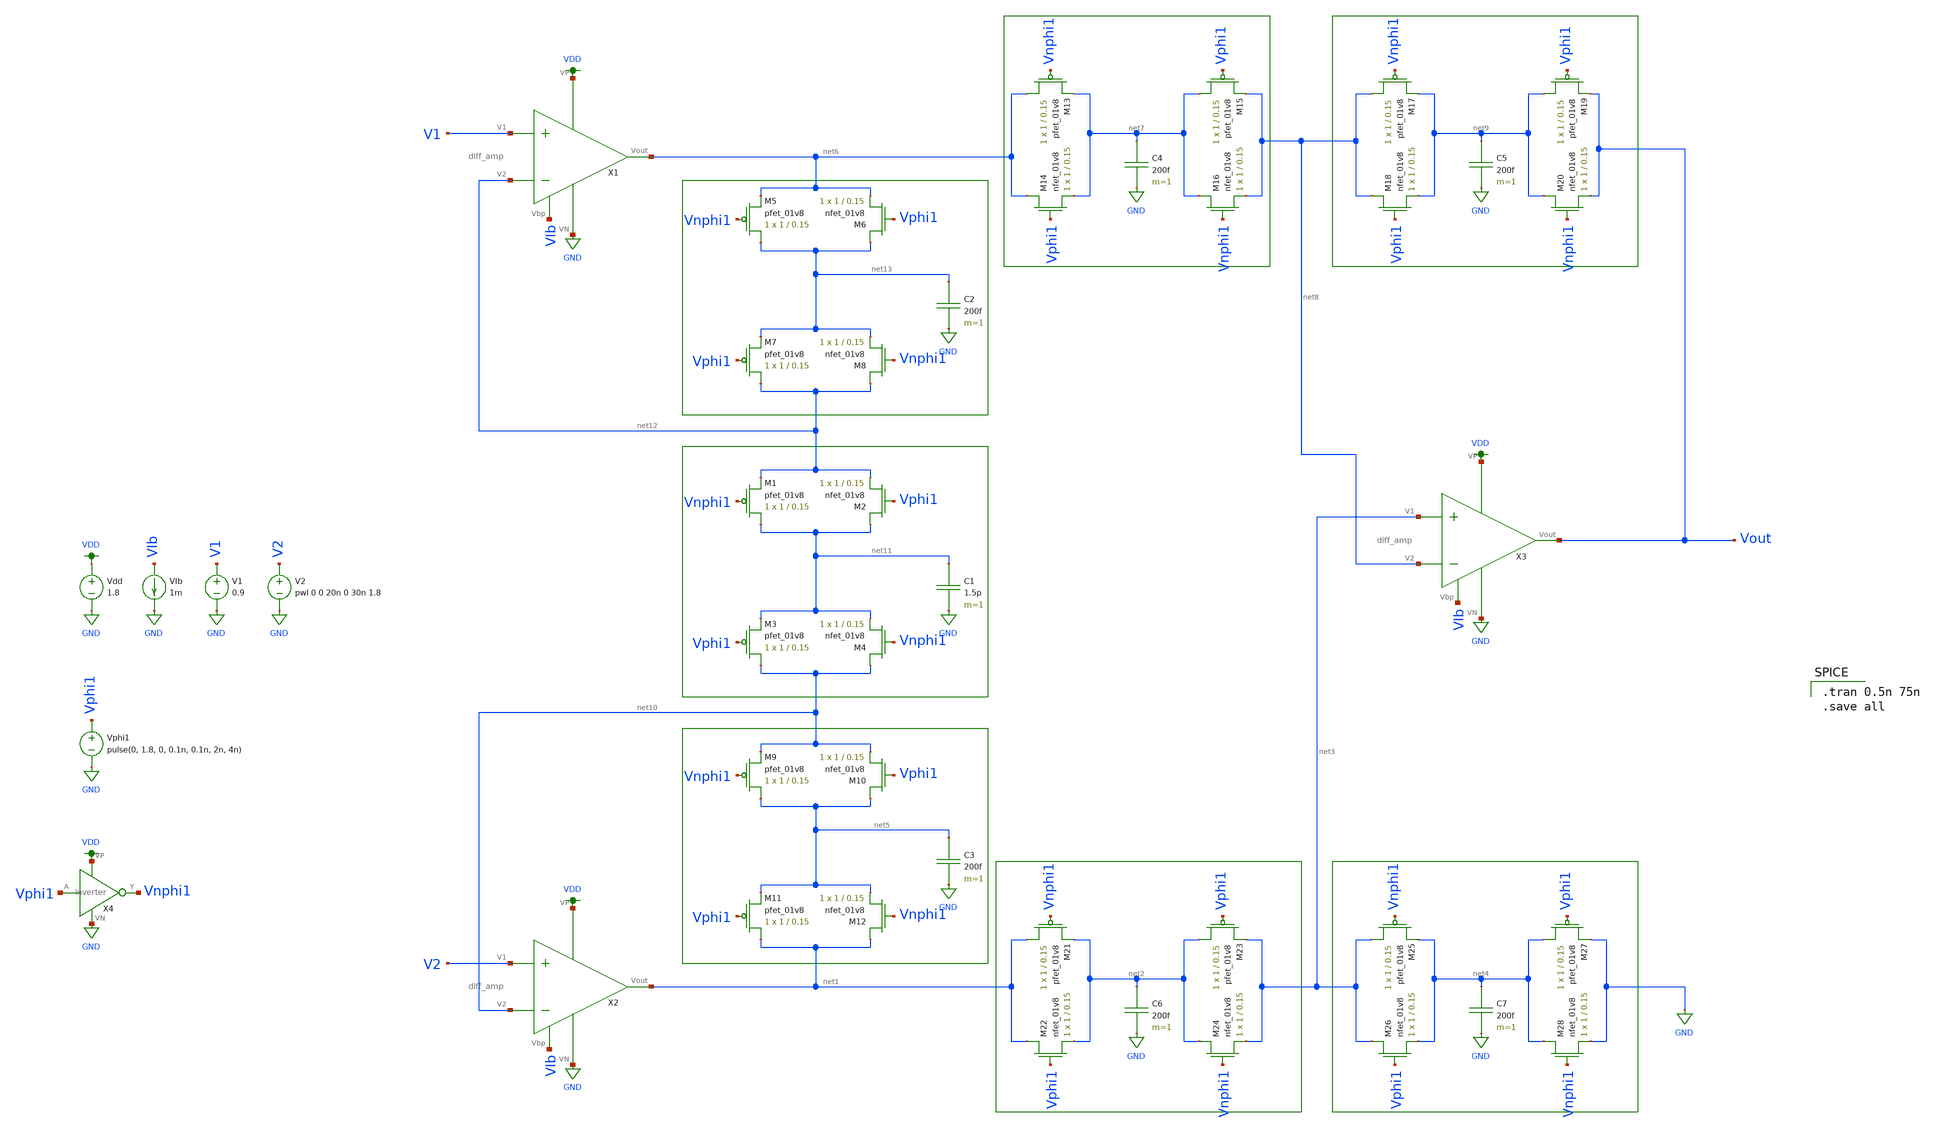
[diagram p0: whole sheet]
** sch_path: schematic/archive/alpha_amp.sch
**.subckt alpha_amp
X1 VDD VIb net6 V1 net12 GND diff_amp
X2 VDD VIb net1 V2 net10 GND diff_amp
X3 VDD VIb Vout net3 net8 GND diff_amp
XM1 net11 Vnphi1 net12 VDD sky130_fd_pr__pfet_01v8 L=0.15 W=1 nf=1 ad='int((nf+1)/2) * W/nf * 0.29' as='int((nf+2)/2) * W/nf * 0.29'
+ pd='2*int((nf+1)/2) * (W/nf + 0.29)' ps='2*int((nf+2)/2) * (W/nf + 0.29)' nrd='0.29 / W' nrs='0.29 / W'
+ sa=0 sb=0 sd=0 mult=1 m=1
XM2 net11 Vphi1 net12 GND sky130_fd_pr__nfet_01v8 L=0.15 W=1 nf=1 ad='int((nf+1)/2) * W/nf * 0.29' as='int((nf+2)/2) * W/nf * 0.29'
+ pd='2*int((nf+1)/2) * (W/nf + 0.29)' ps='2*int((nf+2)/2) * (W/nf + 0.29)' nrd='0.29 / W' nrs='0.29 / W'
+ sa=0 sb=0 sd=0 mult=1 m=1
C1 net11 GND 1.5p m=1
XM3 net10 Vphi1 net11 VDD sky130_fd_pr__pfet_01v8 L=0.15 W=1 nf=1 ad='int((nf+1)/2) * W/nf * 0.29' as='int((nf+2)/2) * W/nf * 0.29'
+ pd='2*int((nf+1)/2) * (W/nf + 0.29)' ps='2*int((nf+2)/2) * (W/nf + 0.29)' nrd='0.29 / W' nrs='0.29 / W'
+ sa=0 sb=0 sd=0 mult=1 m=1
XM4 net10 Vnphi1 net11 GND sky130_fd_pr__nfet_01v8 L=0.15 W=1 nf=1 ad='int((nf+1)/2) * W/nf * 0.29' as='int((nf+2)/2) * W/nf * 0.29'
+ pd='2*int((nf+1)/2) * (W/nf + 0.29)' ps='2*int((nf+2)/2) * (W/nf + 0.29)' nrd='0.29 / W' nrs='0.29 / W'
+ sa=0 sb=0 sd=0 mult=1 m=1
XM5 net13 Vnphi1 net6 VDD sky130_fd_pr__pfet_01v8 L=0.15 W=1 nf=1 ad='int((nf+1)/2) * W/nf * 0.29' as='int((nf+2)/2) * W/nf * 0.29'
+ pd='2*int((nf+1)/2) * (W/nf + 0.29)' ps='2*int((nf+2)/2) * (W/nf + 0.29)' nrd='0.29 / W' nrs='0.29 / W'
+ sa=0 sb=0 sd=0 mult=1 m=1
XM6 net13 Vphi1 net6 GND sky130_fd_pr__nfet_01v8 L=0.15 W=1 nf=1 ad='int((nf+1)/2) * W/nf * 0.29' as='int((nf+2)/2) * W/nf * 0.29'
+ pd='2*int((nf+1)/2) * (W/nf + 0.29)' ps='2*int((nf+2)/2) * (W/nf + 0.29)' nrd='0.29 / W' nrs='0.29 / W'
+ sa=0 sb=0 sd=0 mult=1 m=1
C2 net13 GND 200f m=1
XM7 net12 Vphi1 net13 VDD sky130_fd_pr__pfet_01v8 L=0.15 W=1 nf=1 ad='int((nf+1)/2) * W/nf * 0.29' as='int((nf+2)/2) * W/nf * 0.29'
+ pd='2*int((nf+1)/2) * (W/nf + 0.29)' ps='2*int((nf+2)/2) * (W/nf + 0.29)' nrd='0.29 / W' nrs='0.29 / W'
+ sa=0 sb=0 sd=0 mult=1 m=1
XM8 net12 Vnphi1 net13 GND sky130_fd_pr__nfet_01v8 L=0.15 W=1 nf=1 ad='int((nf+1)/2) * W/nf * 0.29' as='int((nf+2)/2) * W/nf * 0.29'
+ pd='2*int((nf+1)/2) * (W/nf + 0.29)' ps='2*int((nf+2)/2) * (W/nf + 0.29)' nrd='0.29 / W' nrs='0.29 / W'
+ sa=0 sb=0 sd=0 mult=1 m=1
XM9 net5 Vnphi1 net10 VDD sky130_fd_pr__pfet_01v8 L=0.15 W=1 nf=1 ad='int((nf+1)/2) * W/nf * 0.29' as='int((nf+2)/2) * W/nf * 0.29'
+ pd='2*int((nf+1)/2) * (W/nf + 0.29)' ps='2*int((nf+2)/2) * (W/nf + 0.29)' nrd='0.29 / W' nrs='0.29 / W'
+ sa=0 sb=0 sd=0 mult=1 m=1
XM10 net5 Vphi1 net10 GND sky130_fd_pr__nfet_01v8 L=0.15 W=1 nf=1 ad='int((nf+1)/2) * W/nf * 0.29' as='int((nf+2)/2) * W/nf * 0.29'
+ pd='2*int((nf+1)/2) * (W/nf + 0.29)' ps='2*int((nf+2)/2) * (W/nf + 0.29)' nrd='0.29 / W' nrs='0.29 / W'
+ sa=0 sb=0 sd=0 mult=1 m=1
C3 net5 GND 200f m=1
XM11 net1 Vphi1 net5 VDD sky130_fd_pr__pfet_01v8 L=0.15 W=1 nf=1 ad='int((nf+1)/2) * W/nf * 0.29' as='int((nf+2)/2) * W/nf * 0.29'
+ pd='2*int((nf+1)/2) * (W/nf + 0.29)' ps='2*int((nf+2)/2) * (W/nf + 0.29)' nrd='0.29 / W' nrs='0.29 / W'
+ sa=0 sb=0 sd=0 mult=1 m=1
XM12 net1 Vnphi1 net5 GND sky130_fd_pr__nfet_01v8 L=0.15 W=1 nf=1 ad='int((nf+1)/2) * W/nf * 0.29' as='int((nf+2)/2) * W/nf * 0.29'
+ pd='2*int((nf+1)/2) * (W/nf + 0.29)' ps='2*int((nf+2)/2) * (W/nf + 0.29)' nrd='0.29 / W' nrs='0.29 / W'
+ sa=0 sb=0 sd=0 mult=1 m=1
XM13 net6 Vnphi1 net7 VDD sky130_fd_pr__pfet_01v8 L=0.15 W=1 nf=1 ad='int((nf+1)/2) * W/nf * 0.29' as='int((nf+2)/2) * W/nf * 0.29'
+ pd='2*int((nf+1)/2) * (W/nf + 0.29)' ps='2*int((nf+2)/2) * (W/nf + 0.29)' nrd='0.29 / W' nrs='0.29 / W'
+ sa=0 sb=0 sd=0 mult=1 m=1
XM14 net6 Vphi1 net7 GND sky130_fd_pr__nfet_01v8 L=0.15 W=1 nf=1 ad='int((nf+1)/2) * W/nf * 0.29' as='int((nf+2)/2) * W/nf * 0.29'
+ pd='2*int((nf+1)/2) * (W/nf + 0.29)' ps='2*int((nf+2)/2) * (W/nf + 0.29)' nrd='0.29 / W' nrs='0.29 / W'
+ sa=0 sb=0 sd=0 mult=1 m=1
C4 net7 GND 200f m=1
XM15 net7 Vphi1 net8 VDD sky130_fd_pr__pfet_01v8 L=0.15 W=1 nf=1 ad='int((nf+1)/2) * W/nf * 0.29' as='int((nf+2)/2) * W/nf * 0.29'
+ pd='2*int((nf+1)/2) * (W/nf + 0.29)' ps='2*int((nf+2)/2) * (W/nf + 0.29)' nrd='0.29 / W' nrs='0.29 / W'
+ sa=0 sb=0 sd=0 mult=1 m=1
XM16 net7 Vnphi1 net8 GND sky130_fd_pr__nfet_01v8 L=0.15 W=1 nf=1 ad='int((nf+1)/2) * W/nf * 0.29' as='int((nf+2)/2) * W/nf * 0.29'
+ pd='2*int((nf+1)/2) * (W/nf + 0.29)' ps='2*int((nf+2)/2) * (W/nf + 0.29)' nrd='0.29 / W' nrs='0.29 / W'
+ sa=0 sb=0 sd=0 mult=1 m=1
XM17 net8 Vnphi1 net9 VDD sky130_fd_pr__pfet_01v8 L=0.15 W=1 nf=1 ad='int((nf+1)/2) * W/nf * 0.29' as='int((nf+2)/2) * W/nf * 0.29'
+ pd='2*int((nf+1)/2) * (W/nf + 0.29)' ps='2*int((nf+2)/2) * (W/nf + 0.29)' nrd='0.29 / W' nrs='0.29 / W'
+ sa=0 sb=0 sd=0 mult=1 m=1
XM18 net8 Vphi1 net9 GND sky130_fd_pr__nfet_01v8 L=0.15 W=1 nf=1 ad='int((nf+1)/2) * W/nf * 0.29' as='int((nf+2)/2) * W/nf * 0.29'
+ pd='2*int((nf+1)/2) * (W/nf + 0.29)' ps='2*int((nf+2)/2) * (W/nf + 0.29)' nrd='0.29 / W' nrs='0.29 / W'
+ sa=0 sb=0 sd=0 mult=1 m=1
C5 net9 GND 200f m=1
XM19 net9 Vphi1 Vout VDD sky130_fd_pr__pfet_01v8 L=0.15 W=1 nf=1 ad='int((nf+1)/2) * W/nf * 0.29' as='int((nf+2)/2) * W/nf * 0.29'
+ pd='2*int((nf+1)/2) * (W/nf + 0.29)' ps='2*int((nf+2)/2) * (W/nf + 0.29)' nrd='0.29 / W' nrs='0.29 / W'
+ sa=0 sb=0 sd=0 mult=1 m=1
XM20 net9 Vnphi1 Vout GND sky130_fd_pr__nfet_01v8 L=0.15 W=1 nf=1 ad='int((nf+1)/2) * W/nf * 0.29' as='int((nf+2)/2) * W/nf * 0.29'
+ pd='2*int((nf+1)/2) * (W/nf + 0.29)' ps='2*int((nf+2)/2) * (W/nf + 0.29)' nrd='0.29 / W' nrs='0.29 / W'
+ sa=0 sb=0 sd=0 mult=1 m=1
XM21 net1 Vnphi1 net2 VDD sky130_fd_pr__pfet_01v8 L=0.15 W=1 nf=1 ad='int((nf+1)/2) * W/nf * 0.29' as='int((nf+2)/2) * W/nf * 0.29'
+ pd='2*int((nf+1)/2) * (W/nf + 0.29)' ps='2*int((nf+2)/2) * (W/nf + 0.29)' nrd='0.29 / W' nrs='0.29 / W'
+ sa=0 sb=0 sd=0 mult=1 m=1
XM22 net1 Vphi1 net2 GND sky130_fd_pr__nfet_01v8 L=0.15 W=1 nf=1 ad='int((nf+1)/2) * W/nf * 0.29' as='int((nf+2)/2) * W/nf * 0.29'
+ pd='2*int((nf+1)/2) * (W/nf + 0.29)' ps='2*int((nf+2)/2) * (W/nf + 0.29)' nrd='0.29 / W' nrs='0.29 / W'
+ sa=0 sb=0 sd=0 mult=1 m=1
C6 net2 GND 200f m=1
XM23 net2 Vphi1 net3 VDD sky130_fd_pr__pfet_01v8 L=0.15 W=1 nf=1 ad='int((nf+1)/2) * W/nf * 0.29' as='int((nf+2)/2) * W/nf * 0.29'
+ pd='2*int((nf+1)/2) * (W/nf + 0.29)' ps='2*int((nf+2)/2) * (W/nf + 0.29)' nrd='0.29 / W' nrs='0.29 / W'
+ sa=0 sb=0 sd=0 mult=1 m=1
XM24 net2 Vnphi1 net3 GND sky130_fd_pr__nfet_01v8 L=0.15 W=1 nf=1 ad='int((nf+1)/2) * W/nf * 0.29' as='int((nf+2)/2) * W/nf * 0.29'
+ pd='2*int((nf+1)/2) * (W/nf + 0.29)' ps='2*int((nf+2)/2) * (W/nf + 0.29)' nrd='0.29 / W' nrs='0.29 / W'
+ sa=0 sb=0 sd=0 mult=1 m=1
XM25 net3 Vnphi1 net4 VDD sky130_fd_pr__pfet_01v8 L=0.15 W=1 nf=1 ad='int((nf+1)/2) * W/nf * 0.29' as='int((nf+2)/2) * W/nf * 0.29'
+ pd='2*int((nf+1)/2) * (W/nf + 0.29)' ps='2*int((nf+2)/2) * (W/nf + 0.29)' nrd='0.29 / W' nrs='0.29 / W'
+ sa=0 sb=0 sd=0 mult=1 m=1
XM26 net3 Vphi1 net4 GND sky130_fd_pr__nfet_01v8 L=0.15 W=1 nf=1 ad='int((nf+1)/2) * W/nf * 0.29' as='int((nf+2)/2) * W/nf * 0.29'
+ pd='2*int((nf+1)/2) * (W/nf + 0.29)' ps='2*int((nf+2)/2) * (W/nf + 0.29)' nrd='0.29 / W' nrs='0.29 / W'
+ sa=0 sb=0 sd=0 mult=1 m=1
C7 net4 GND 200f m=1
XM27 net4 Vphi1 GND VDD sky130_fd_pr__pfet_01v8 L=0.15 W=1 nf=1 ad='int((nf+1)/2) * W/nf * 0.29' as='int((nf+2)/2) * W/nf * 0.29'
+ pd='2*int((nf+1)/2) * (W/nf + 0.29)' ps='2*int((nf+2)/2) * (W/nf + 0.29)' nrd='0.29 / W' nrs='0.29 / W'
+ sa=0 sb=0 sd=0 mult=1 m=1
XM28 net4 Vnphi1 GND GND sky130_fd_pr__nfet_01v8 L=0.15 W=1 nf=1 ad='int((nf+1)/2) * W/nf * 0.29' as='int((nf+2)/2) * W/nf * 0.29'
+ pd='2*int((nf+1)/2) * (W/nf + 0.29)' ps='2*int((nf+2)/2) * (W/nf + 0.29)' nrd='0.29 / W' nrs='0.29 / W'
+ sa=0 sb=0 sd=0 mult=1 m=1
Vdd VDD GND 1.8
V1 V1 GND 0.9
V2 V2 GND pwl 0 0 20n 0 30n 1.8
Vphi1 Vphi1 GND pulse(0, 1.8, 0, 0.1n, 0.1n, 2n, 4n)
VIb VIb GND 1m
X4 Vphi1 Vnphi1 VDD GND inverter
**** begin user architecture code

.option wnflag=1
.param MC_SWITCH=0.0
.lib ~/skywater/skywater-pdk/libraries/sky130_fd_pr_ngspice/latest/models/sky130.lib.spice tt


.tran 0.5n 75n
.save all

**** end user architecture code
**.ends
.GLOBAL GND
.GLOBAL VDD
.end
